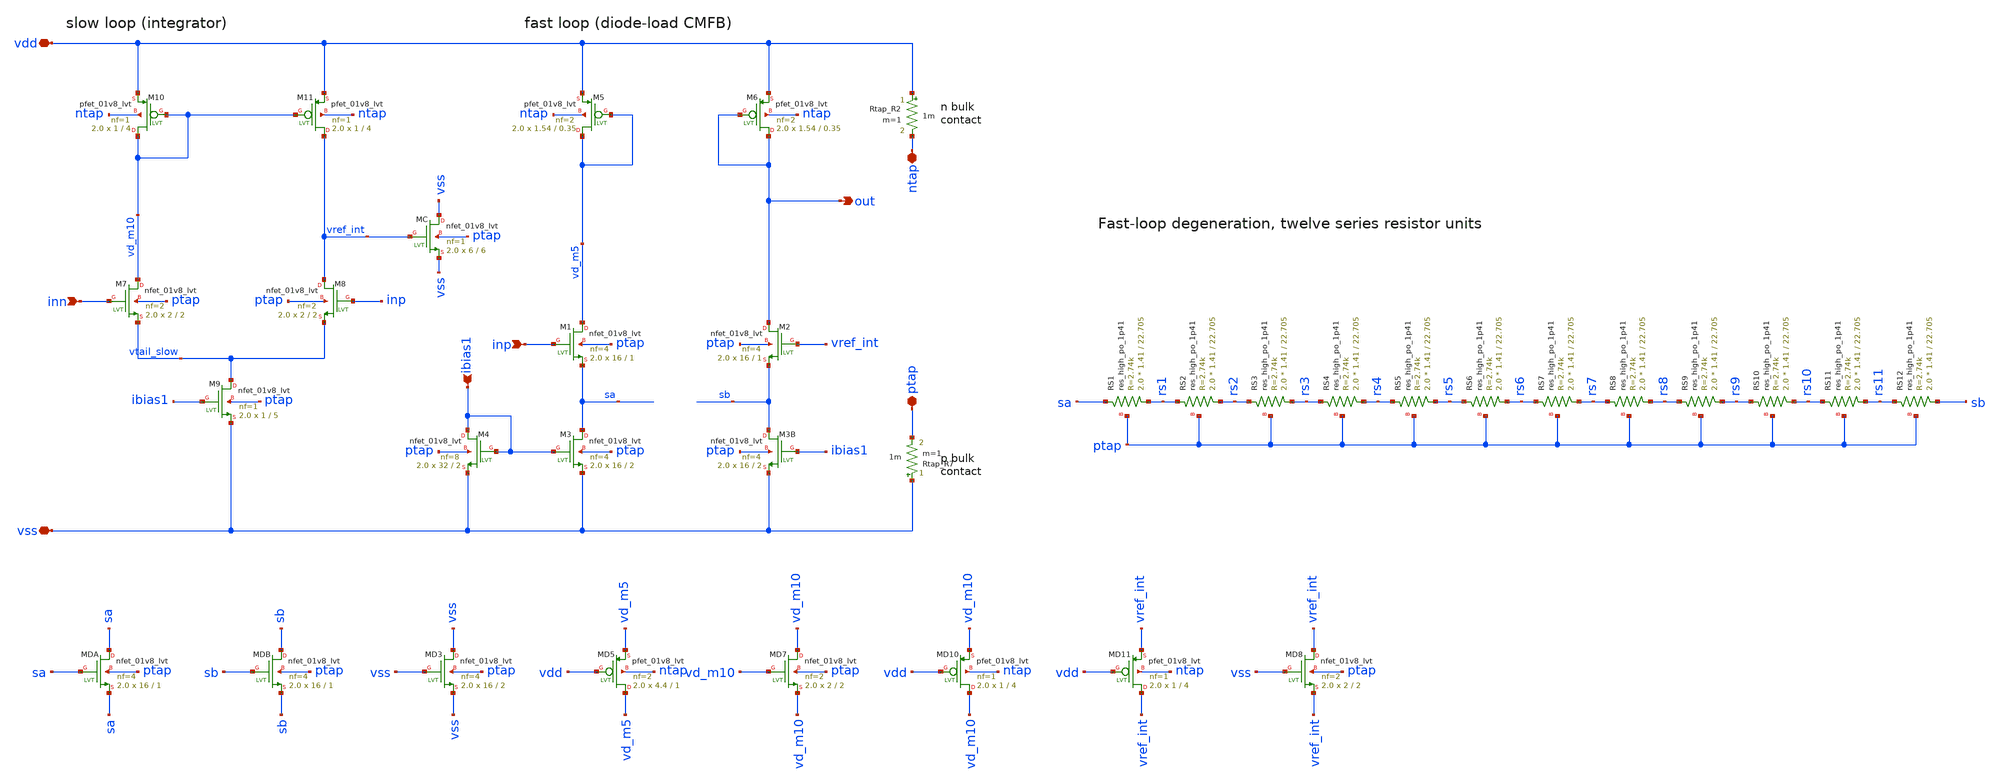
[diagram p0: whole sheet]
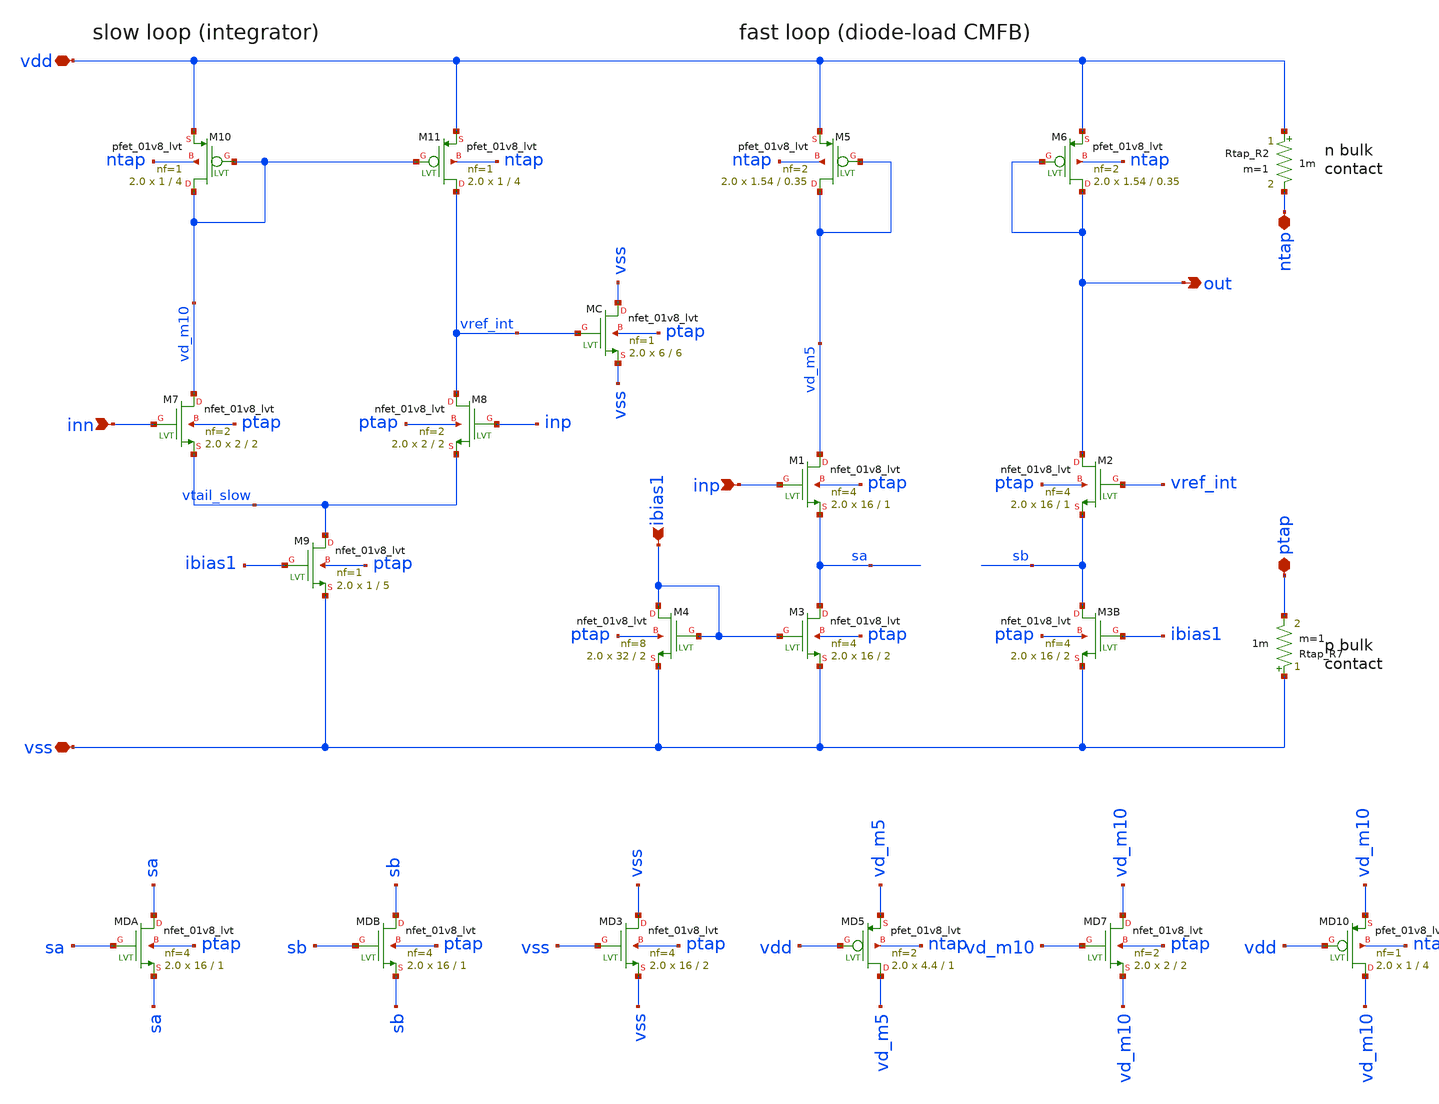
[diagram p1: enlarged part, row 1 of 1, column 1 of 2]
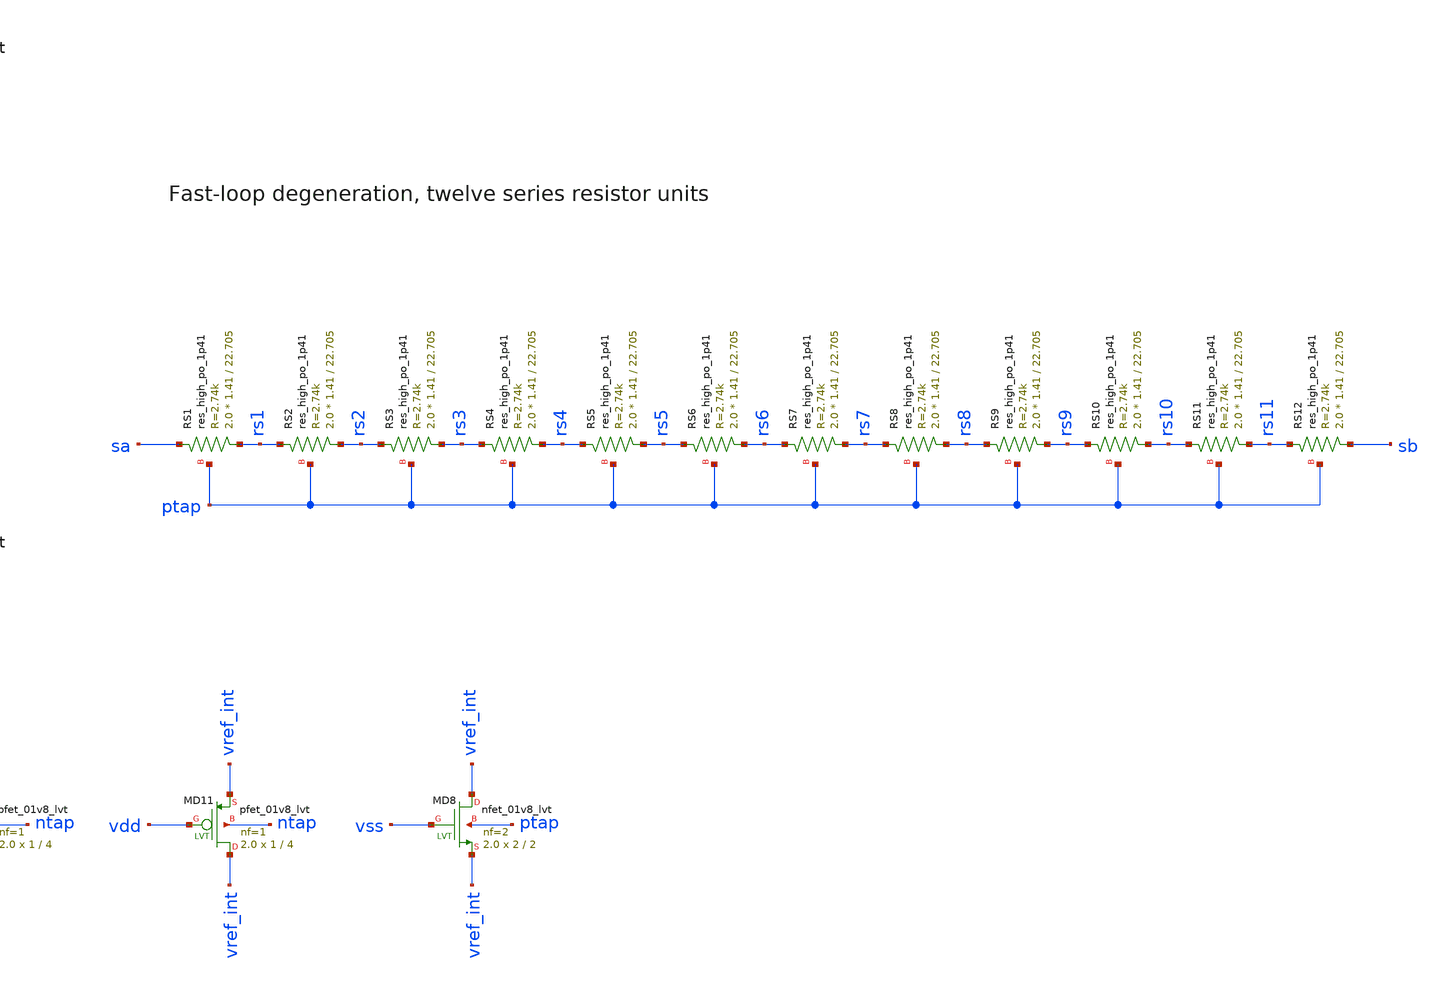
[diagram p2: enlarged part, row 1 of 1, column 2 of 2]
** sch_path: verification/porting/sky_replica_schematic/schematic/ota.sch
**.subckt ota out inp ibias1 inn ntap ptap vdd vss
*.opin out
*.ipin inp
*.ipin ibias1
*.ipin inn
*.iopin ntap
*.iopin ptap
*.iopin vdd
*.iopin vss
XM5 vd_m5 vd_m5 vdd ntap sky130_fd_pr__pfet_01v8_lvt L=0.35 W=1.54 nf=2 ad=0.2233 as=0.4466 pd=2.12
+ ps=4.24 nrd=0.1883116883116883 nrs=0.1883116883116883 sa=0 sb=0 sd=0 mult=2.0 m=2.0
XM6 out out vdd ntap sky130_fd_pr__pfet_01v8_lvt L=0.35 W=1.54 nf=2 ad=0.2233 as=0.4466 pd=2.12
+ ps=4.24 nrd=0.1883116883116883 nrs=0.1883116883116883 sa=0 sb=0 sd=0 mult=2.0 m=2.0
XM1 vd_m5 inp sa ptap sky130_fd_pr__nfet_01v8_lvt L=1 W=16 nf=4 ad=2.32 as=3.48 pd=17.16 ps=25.74
+ nrd=0.018125 nrs=0.018125 sa=0 sb=0 sd=0 mult=2.0 m=2.0
XM2 out vref_int sb ptap sky130_fd_pr__nfet_01v8_lvt L=1 W=16 nf=4 ad=2.32 as=3.48 pd=17.16 ps=25.74
+ nrd=0.018125 nrs=0.018125 sa=0 sb=0 sd=0 mult=2.0 m=2.0
XRS1 rs1 sa ptap sky130_fd_pr__res_high_po_1p41 L=22.705 mult=2.0 m=2.0
XRS2 rs2 rs1 ptap sky130_fd_pr__res_high_po_1p41 L=22.705 mult=2.0 m=2.0
XRS3 rs3 rs2 ptap sky130_fd_pr__res_high_po_1p41 L=22.705 mult=2.0 m=2.0
XRS4 rs4 rs3 ptap sky130_fd_pr__res_high_po_1p41 L=22.705 mult=2.0 m=2.0
XRS5 rs5 rs4 ptap sky130_fd_pr__res_high_po_1p41 L=22.705 mult=2.0 m=2.0
XRS6 rs6 rs5 ptap sky130_fd_pr__res_high_po_1p41 L=22.705 mult=2.0 m=2.0
XRS7 rs7 rs6 ptap sky130_fd_pr__res_high_po_1p41 L=22.705 mult=2.0 m=2.0
XRS8 rs8 rs7 ptap sky130_fd_pr__res_high_po_1p41 L=22.705 mult=2.0 m=2.0
XRS9 rs9 rs8 ptap sky130_fd_pr__res_high_po_1p41 L=22.705 mult=2.0 m=2.0
XRS10 rs10 rs9 ptap sky130_fd_pr__res_high_po_1p41 L=22.705 mult=2.0 m=2.0
XRS11 rs11 rs10 ptap sky130_fd_pr__res_high_po_1p41 L=22.705 mult=2.0 m=2.0
XRS12 sb rs11 ptap sky130_fd_pr__res_high_po_1p41 L=22.705 mult=2.0 m=2.0
XM3 sa ibias1 vss ptap sky130_fd_pr__nfet_01v8_lvt L=2 W=16 nf=4 ad=2.32 as=3.48 pd=17.16 ps=25.74
+ nrd=0.018125 nrs=0.018125 sa=0 sb=0 sd=0 mult=2.0 m=2.0
XM3B sb ibias1 vss ptap sky130_fd_pr__nfet_01v8_lvt L=2 W=16 nf=4 ad=2.32 as=3.48 pd=17.16 ps=25.74
+ nrd=0.018125 nrs=0.018125 sa=0 sb=0 sd=0 mult=2.0 m=2.0
XM4 ibias1 ibias1 vss ptap sky130_fd_pr__nfet_01v8_lvt L=2 W=32 nf=8 ad=4.64 as=5.8 pd=34.32 ps=42.9
+ nrd=0.0090625 nrs=0.0090625 sa=0 sb=0 sd=0 mult=2.0 m=2.0
XM10 vd_m10 vd_m10 vdd ntap sky130_fd_pr__pfet_01v8_lvt L=4 W=1 nf=1 ad=0.29 as=0.29 pd=2.58 ps=2.58
+ nrd=0.29 nrs=0.29 sa=0 sb=0 sd=0 mult=2.0 m=2.0
XM11 vref_int vd_m10 vdd ntap sky130_fd_pr__pfet_01v8_lvt L=4 W=1 nf=1 ad=0.29 as=0.29 pd=2.58
+ ps=2.58 nrd=0.29 nrs=0.29 sa=0 sb=0 sd=0 mult=2.0 m=2.0
XM7 vd_m10 inn vtail_slow ptap sky130_fd_pr__nfet_01v8_lvt L=2 W=2 nf=2 ad=0.29 as=0.58 pd=2.58
+ ps=5.16 nrd=0.145 nrs=0.145 sa=0 sb=0 sd=0 mult=2.0 m=2.0
XM8 vref_int inp vtail_slow ptap sky130_fd_pr__nfet_01v8_lvt L=2 W=2 nf=2 ad=0.29 as=0.58 pd=2.58
+ ps=5.16 nrd=0.145 nrs=0.145 sa=0 sb=0 sd=0 mult=2.0 m=2.0
XM9 vtail_slow ibias1 vss ptap sky130_fd_pr__nfet_01v8_lvt L=5 W=1 nf=1 ad=0.29 as=0.29 pd=2.58
+ ps=2.58 nrd=0.29 nrs=0.29 sa=0 sb=0 sd=0 mult=2.0 m=2.0
XMC vss vref_int vss ptap sky130_fd_pr__nfet_01v8_lvt L=6 W=6 nf=1 ad=1.74 as=1.74 pd=12.58 ps=12.58
+ nrd=0.04833333333333333 nrs=0.04833333333333333 sa=0 sb=0 sd=0 mult=2.0 m=2.0
Rtap_R2 vdd ntap 1m m=1
Rtap_R7 vss ptap 1m m=1
XMDA sa sa sa ptap sky130_fd_pr__nfet_01v8_lvt L=1 W=16 nf=4 ad=2.32 as=3.48 pd=17.16 ps=25.74
+ nrd=0.018125 nrs=0.018125 sa=0 sb=0 sd=0 mult=2.0 m=2.0
XMDB sb sb sb ptap sky130_fd_pr__nfet_01v8_lvt L=1 W=16 nf=4 ad=2.32 as=3.48 pd=17.16 ps=25.74
+ nrd=0.018125 nrs=0.018125 sa=0 sb=0 sd=0 mult=2.0 m=2.0
XMD3 vss vss vss ptap sky130_fd_pr__nfet_01v8_lvt L=2 W=16 nf=4 ad=2.32 as=3.48 pd=17.16 ps=25.74
+ nrd=0.018125 nrs=0.018125 sa=0 sb=0 sd=0 mult=2.0 m=2.0
XMD5 vd_m5 vdd vd_m5 ntap sky130_fd_pr__pfet_01v8_lvt L=1 W=4.4 nf=2 ad=0.638 as=1.276 pd=4.98
+ ps=9.96 nrd=0.0659090909090909 nrs=0.0659090909090909 sa=0 sb=0 sd=0 mult=2.0 m=2.0
XMD7 vd_m10 vd_m10 vd_m10 ptap sky130_fd_pr__nfet_01v8_lvt L=2 W=2 nf=2 ad=0.29 as=0.58 pd=2.58
+ ps=5.16 nrd=0.145 nrs=0.145 sa=0 sb=0 sd=0 mult=2.0 m=2.0
XMD10 vd_m10 vdd vd_m10 ntap sky130_fd_pr__pfet_01v8_lvt L=4 W=1 nf=1 ad=0.29 as=0.29 pd=2.58
+ ps=2.58 nrd=0.29 nrs=0.29 sa=0 sb=0 sd=0 mult=2.0 m=2.0
XMD11 vref_int vdd vref_int ntap sky130_fd_pr__pfet_01v8_lvt L=4 W=1 nf=1 ad=0.29 as=0.29 pd=2.58
+ ps=2.58 nrd=0.29 nrs=0.29 sa=0 sb=0 sd=0 mult=2.0 m=2.0
XMD8 vref_int vss vref_int ptap sky130_fd_pr__nfet_01v8_lvt L=2 W=2 nf=2 ad=0.29 as=0.58 pd=2.58
+ ps=5.16 nrd=0.145 nrs=0.145 sa=0 sb=0 sd=0 mult=2.0 m=2.0
**.ends
.end
